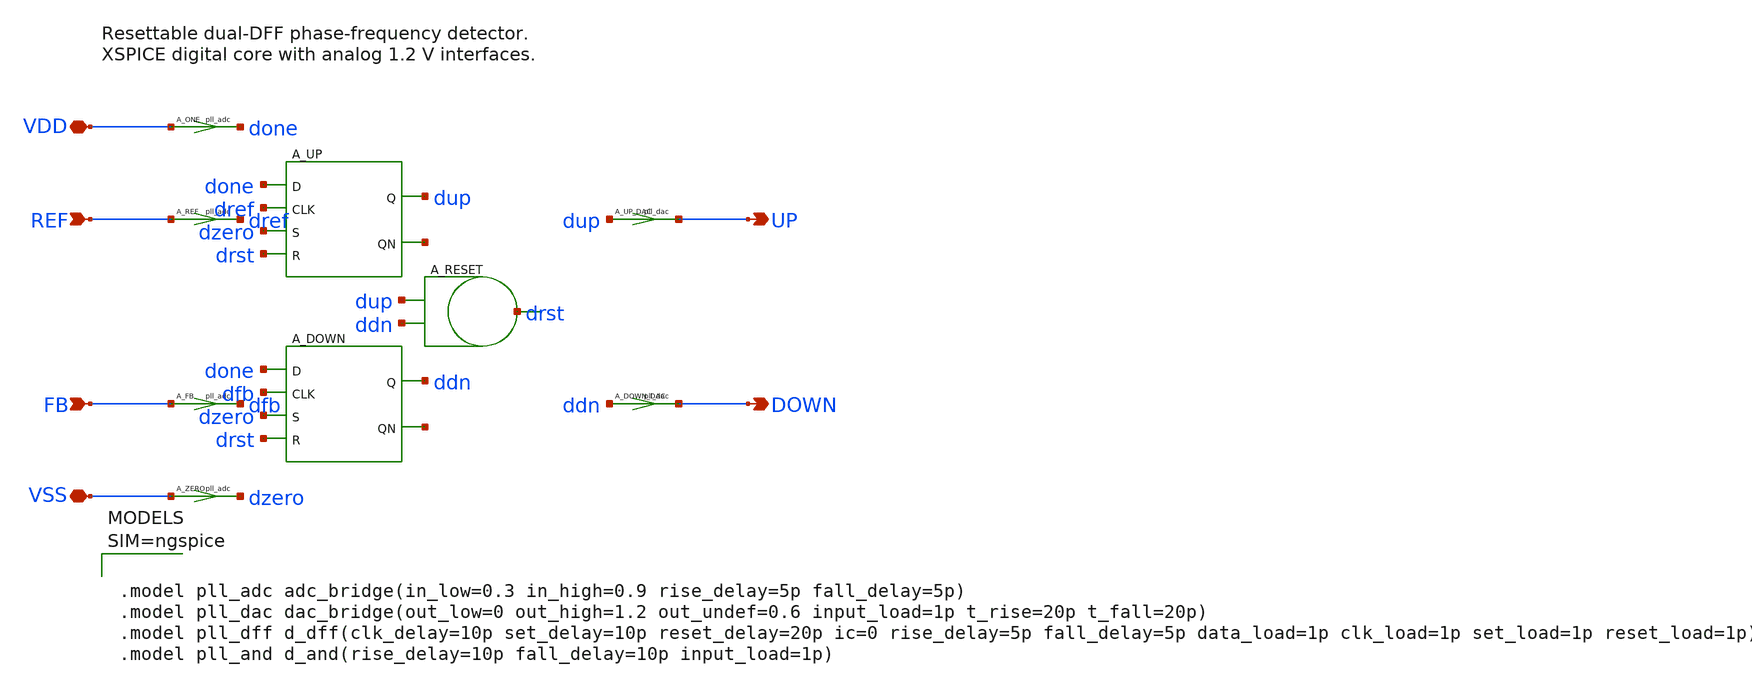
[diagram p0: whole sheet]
** sch_path: macros/pll_analog/schematic/xschem/pfd.sch
**.subckt pfd REF FB UP DOWN VDD VSS
*.ipin REF
*.ipin FB
*.opin UP
*.opin DOWN
*.iopin VDD
*.iopin VSS
A_REF [ REF ] [ dref ] pll_adc
A_FB [ FB ] [ dfb ] pll_adc
A_ONE [ VDD ] [ done ] pll_adc
A_ZERO [ VSS ] [ dzero ] pll_adc
A_UP done dref dzero drst dup net1 pll_dff
A_DOWN done dfb dzero drst ddn net2 pll_dff
A_RESET [ dup ddn ] drst pll_and
A_UP_DAC [ dup ] [ UP ] pll_dac
A_DOWN_DAC [ ddn ] [ DOWN ] pll_dac
**** begin user architecture code



.model pll_adc adc_bridge(in_low=0.3 in_high=0.9 rise_delay=5p fall_delay=5p)
.model pll_dac dac_bridge(out_low=0 out_high=1.2 out_undef=0.6 input_load=1p t_rise=20p t_fall=20p)
.model pll_dff d_dff(clk_delay=10p set_delay=10p reset_delay=20p ic=0 rise_delay=5p fall_delay=5p
+ data_load=1p clk_load=1p set_load=1p reset_load=1p)
.model pll_and d_and(rise_delay=10p fall_delay=10p input_load=1p)



**** end user architecture code
**.ends
.end
